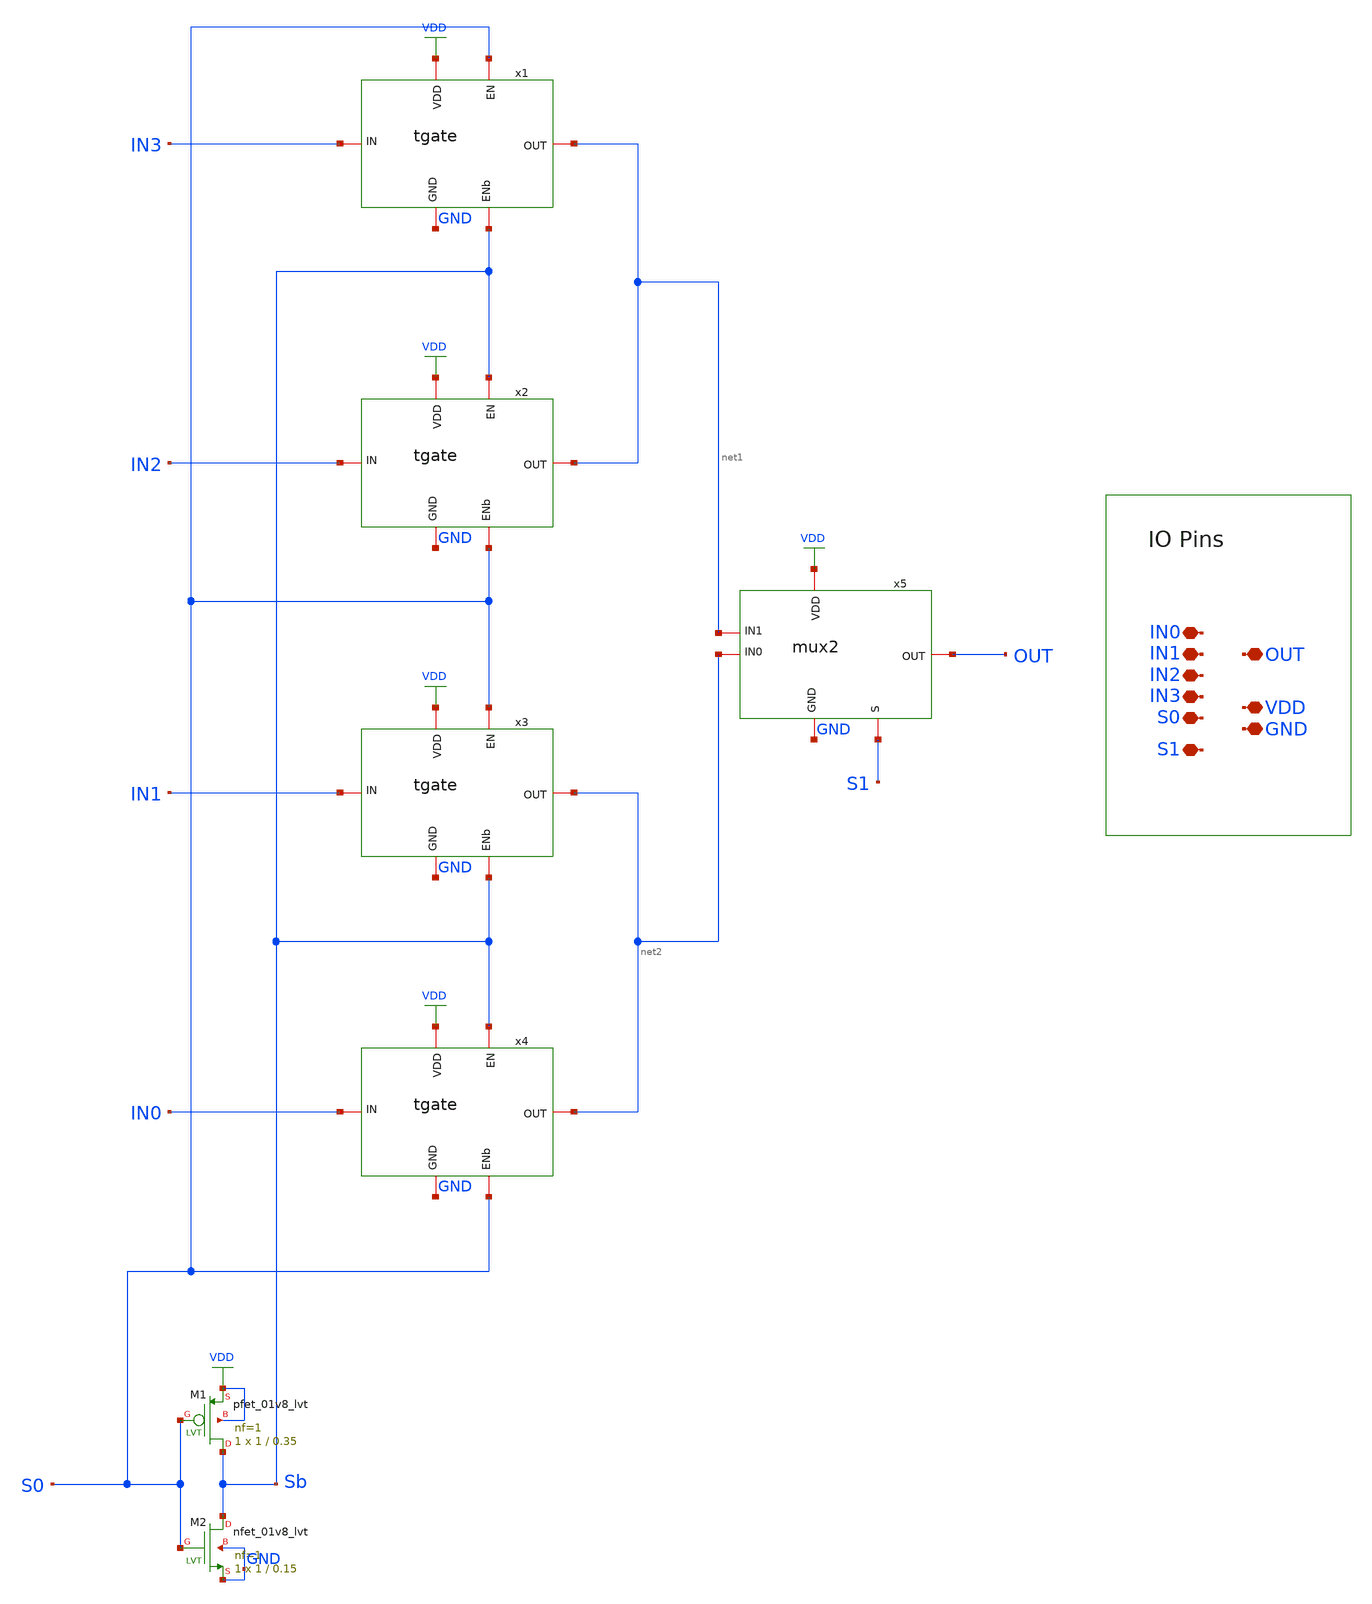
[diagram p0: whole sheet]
** sch_path: scope_sky130_v1/mux4.sch
**.subckt mux4 IN3 VDD GND S0 OUT IN2 IN1 IN0 S1
*.iopin IN3
*.iopin VDD
*.iopin GND
*.iopin S0
*.iopin OUT
*.iopin IN2
*.iopin IN1
*.iopin IN0
*.iopin S1
XM1 Sb S0 VDD VDD sky130_fd_pr__pfet_01v8_lvt L=0.35 W=1 nf=1 ad='int((1 + 1)/2) * 1 / 1 * 0.29' as='int((1 + 2)/2) * 1 / 1 * 0.29'
+ pd='2*int((1 + 1)/2) * (1 / 1 + 0.29)' ps='2*int((1 + 2)/2) * (1 / 1 + 0.29)' nrd='0.29 / 1 ' nrs='0.29 / 1 '
+ sa=0 sb=0 sd=0 mult=1 m=1
XM2 Sb S0 GND GND sky130_fd_pr__nfet_01v8_lvt L=0.15 W=1 nf=1 ad='int((1 + 1)/2) * 1 / 1 * 0.29' as='int((1 + 2)/2) * 1 / 1 * 0.29'
+ pd='2*int((1 + 1)/2) * (1 / 1 + 0.29)' ps='2*int((1 + 2)/2) * (1 / 1 + 0.29)' nrd='0.29 / 1 ' nrs='0.29 / 1 '
+ sa=0 sb=0 sd=0 mult=1 m=1
x1 IN3 net1 Sb S0 VDD GND tgate
x2 IN2 net1 S0 Sb VDD GND tgate
x3 IN1 net2 Sb S0 VDD GND tgate
x4 IN0 net2 S0 Sb VDD GND tgate
x5 net2 net1 S1 OUT VDD GND mux2
**.ends

* expanding   symbol:  scope_sky130_v1/tgate.sym # of pins=6
** sym_path: scope_sky130_v1/tgate.sym
** sch_path: scope_sky130_v1/tgate.sch
.subckt tgate IN OUT ENb EN VDD GND
*.iopin IN
*.iopin VDD
*.iopin GND
*.iopin ENb
*.iopin EN
*.iopin OUT
XM2 IN EN OUT GND sky130_fd_pr__nfet_01v8 L=0.15 W=0.5 nf=1 ad='int((1 + 1)/2) * 0.5 / 1 * 0.29' as='int((1 + 2)/2) * 0.5 / 1 * 0.29'
+ pd='2*int((1 + 1)/2) * (0.5 / 1 + 0.29)' ps='2*int((1 + 2)/2) * (0.5 / 1 + 0.29)' nrd='0.29 / 0.5 ' nrs='0.29 / 0.5 '
+ sa=0 sb=0 sd=0 mult=1 m=1
XM11 IN ENb OUT VDD sky130_fd_pr__pfet_01v8 L=0.15 W=0.5 nf=1 ad='int((nf+1)/2) * W/nf * 0.29' as='int((nf+2)/2) * W/nf * 0.29'
+ pd='2*int((nf+1)/2) * (W/nf + 0.29)' ps='2*int((nf+2)/2) * (W/nf + 0.29)' nrd='0.29 / W' nrs='0.29 / W'
+ sa=0 sb=0 sd=0 mult=1 m=1
.ends


* expanding   symbol:  scope_sky130_v1/mux2.sym # of pins=6
** sym_path: scope_sky130_v1/mux2.sym
** sch_path: scope_sky130_v1/mux2.sch
.subckt mux2 IN0 IN1 S OUT VDD GND
*.iopin IN1
*.iopin VDD
*.iopin GND
*.iopin S
*.iopin OUT
*.iopin IN0
XM1 Sb S VDD VDD sky130_fd_pr__pfet_01v8_lvt L=0.35 W=1 nf=1 ad='int((1 + 1)/2) * 1 / 1 * 0.29' as='int((1 + 2)/2) * 1 / 1 * 0.29'
+ pd='2*int((1 + 1)/2) * (1 / 1 + 0.29)' ps='2*int((1 + 2)/2) * (1 / 1 + 0.29)' nrd='0.29 / 1 ' nrs='0.29 / 1 '
+ sa=0 sb=0 sd=0 mult=1 m=1
XM2 Sb S GND GND sky130_fd_pr__nfet_01v8_lvt L=0.15 W=1 nf=1 ad='int((1 + 1)/2) * 1 / 1 * 0.29' as='int((1 + 2)/2) * 1 / 1 * 0.29'
+ pd='2*int((1 + 1)/2) * (1 / 1 + 0.29)' ps='2*int((1 + 2)/2) * (1 / 1 + 0.29)' nrd='0.29 / 1 ' nrs='0.29 / 1 '
+ sa=0 sb=0 sd=0 mult=1 m=1
x1 IN1 OUT Sb S VDD GND tgate
x2 IN0 OUT S Sb VDD GND tgate
.ends

.GLOBAL VDD
.end
